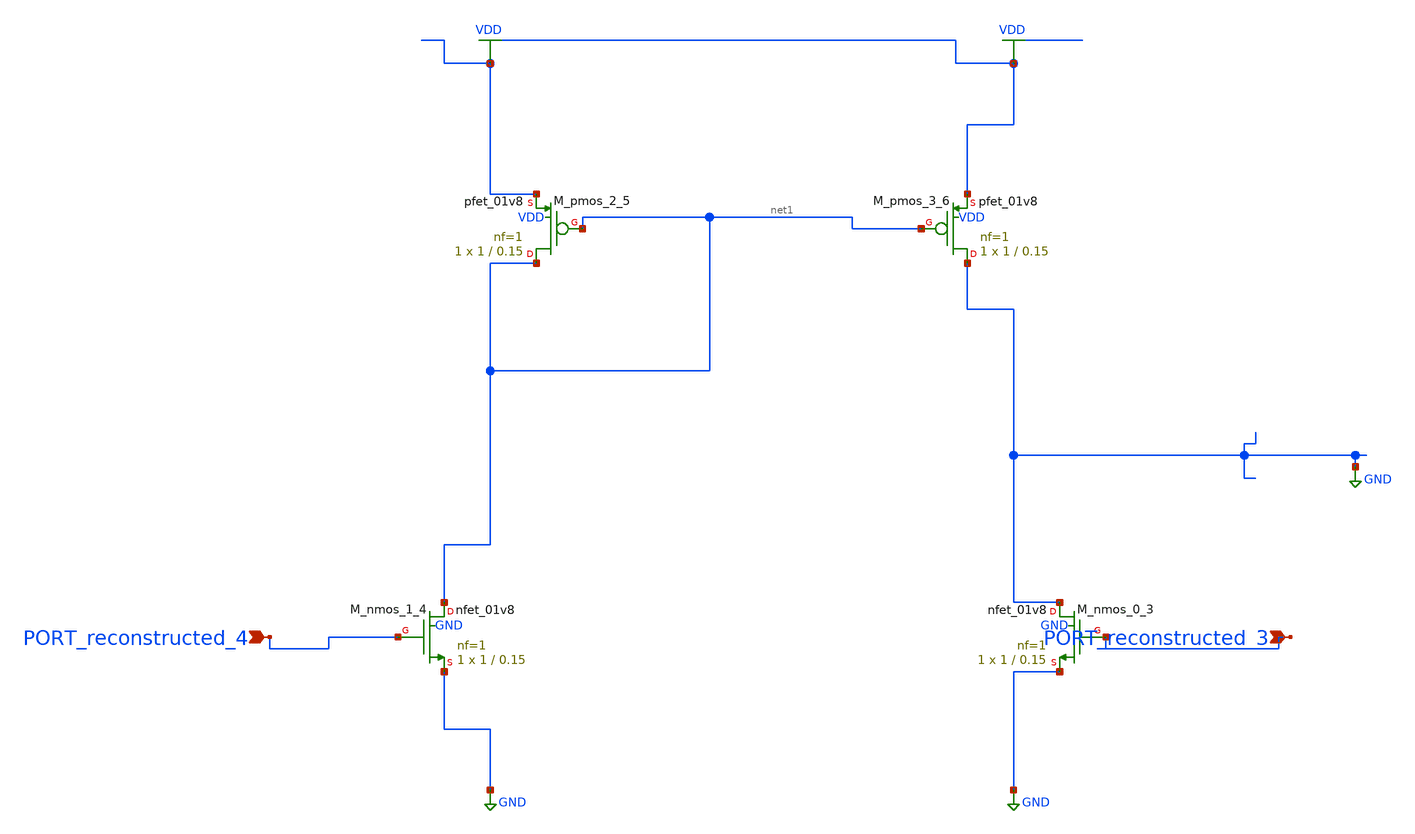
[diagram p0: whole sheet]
** sch_path: schematics/AMSNet/282.sch
**.subckt 282 PORT_reconstructed_3 PORT_reconstructed_4
*.ipin PORT_reconstructed_3
*.ipin PORT_reconstructed_4
XM_nmos_0_3 GND PORT_reconstructed_3 GND GND sky130_fd_pr__nfet_01v8 L=0.15 W=1 nf=1 ad='int((1 + 1)/2) * 1 / 1 * 0.29'
+ as='int((1 + 2)/2) * 1 / 1 * 0.29' pd='2*int((1 + 1)/2) * (1 / 1 + 0.29)' ps='2*int((1 + 2)/2) * (1 / 1 + 0.29)'
+ nrd='0.29 / 1 ' nrs='0.29 / 1 ' sa=0 sb=0 sd=0 mult=1 m=1
XM_nmos_1_4 net1 PORT_reconstructed_4 GND GND sky130_fd_pr__nfet_01v8 L=0.15 W=1 nf=1 ad='int((1 + 1)/2) * 1 / 1 * 0.29'
+ as='int((1 + 2)/2) * 1 / 1 * 0.29' pd='2*int((1 + 1)/2) * (1 / 1 + 0.29)' ps='2*int((1 + 2)/2) * (1 / 1 + 0.29)'
+ nrd='0.29 / 1 ' nrs='0.29 / 1 ' sa=0 sb=0 sd=0 mult=1 m=1
XM_pmos_2_5 net1 net1 VDD VDD sky130_fd_pr__pfet_01v8 L=0.15 W=1 nf=1 ad='int((1 + 1)/2) * 1 / 1 * 0.29'
+ as='int((1 + 2)/2) * 1 / 1 * 0.29' pd='2*int((1 + 1)/2) * (1 / 1 + 0.29)' ps='2*int((1 + 2)/2) * (1 / 1 + 0.29)'
+ nrd='0.29 / 1 ' nrs='0.29 / 1 ' sa=0 sb=0 sd=0 mult=1 m=1
XM_pmos_3_6 GND net1 VDD VDD sky130_fd_pr__pfet_01v8 L=0.15 W=1 nf=1 ad='int((1 + 1)/2) * 1 / 1 * 0.29'
+ as='int((1 + 2)/2) * 1 / 1 * 0.29' pd='2*int((1 + 1)/2) * (1 / 1 + 0.29)' ps='2*int((1 + 2)/2) * (1 / 1 + 0.29)'
+ nrd='0.29 / 1 ' nrs='0.29 / 1 ' sa=0 sb=0 sd=0 mult=1 m=1
**.ends
.GLOBAL GND
.GLOBAL VDD
.end
